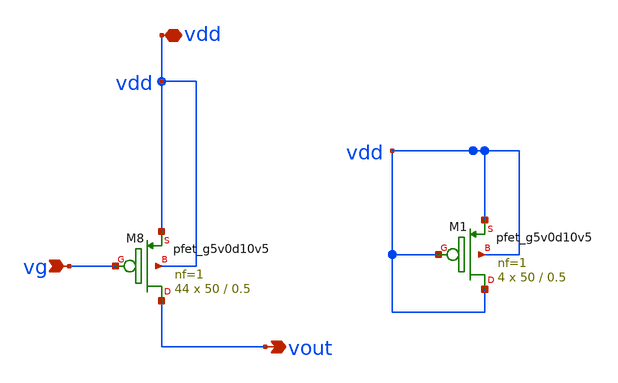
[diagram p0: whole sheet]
** sch_path: schematic/pmosx.sch
**.subckt pmosx vout vdd vg
*.opin vout
*.iopin vdd
*.ipin vg
XM8 vout vg vdd vdd sky130_fd_pr__pfet_g5v0d10v5 L=0.5 W=50 nf=1 ad='int((nf+1)/2) * W/nf * 0.29' as='int((nf+2)/2) * W/nf * 0.29'
+ pd='2*int((nf+1)/2) * (W/nf + 0.29)' ps='2*int((nf+2)/2) * (W/nf + 0.29)' nrd='0.29 / W' nrs='0.29 / W'
+ sa=0 sb=0 sd=0 mult=44 m=44
XM1 vdd vdd vdd vdd sky130_fd_pr__pfet_g5v0d10v5 L=0.5 W=50 nf=1 ad='int((nf+1)/2) * W/nf * 0.29' as='int((nf+2)/2) * W/nf * 0.29'
+ pd='2*int((nf+1)/2) * (W/nf + 0.29)' ps='2*int((nf+2)/2) * (W/nf + 0.29)' nrd='0.29 / W' nrs='0.29 / W'
+ sa=0 sb=0 sd=0 mult=4 m=4
**.ends
.end
